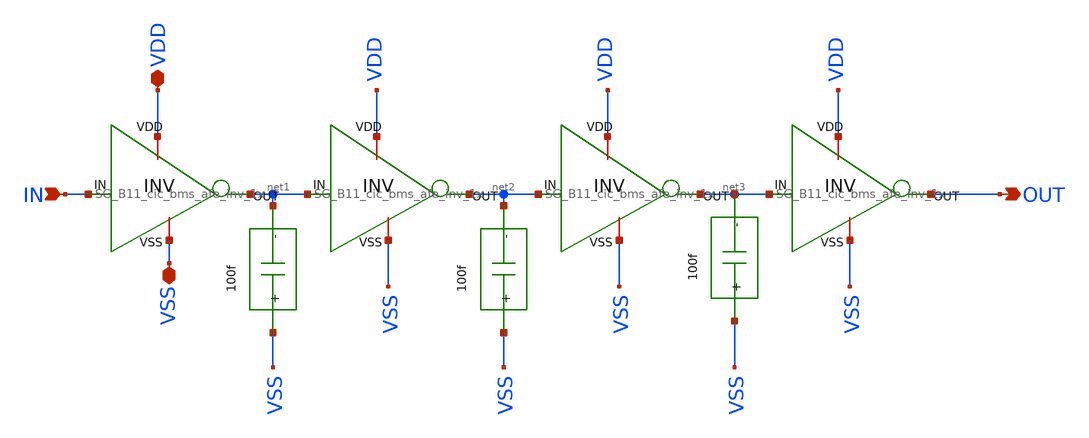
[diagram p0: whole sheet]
** sch_path: design/schematics/NOCG/SG_B11_cic_bms_afe_delay_block_3n.sch
**.subckt SG_B11_cic_bms_afe_delay_block_3n IN OUT VDD VSS
*.ipin IN
*.opin OUT
*.iopin VDD
*.iopin VSS
x1 VDD net1 IN VSS SG_B11_cic_bms_afe_inv_1x
x2 VDD net2 net1 VSS SG_B11_cic_bms_afe_inv_1x
x3 VDD net3 net2 VSS SG_B11_cic_bms_afe_inv_1x
x4 VDD OUT net3 VSS SG_B11_cic_bms_afe_inv_1x
x5 VSS net1 SG_B11_cic_bms_afe_delay_3n_cap
x6 VSS net2 SG_B11_cic_bms_afe_delay_3n_cap
x7 VSS net3 SG_B11_cic_bms_afe_delay_3n_cap
**.ends
.end
